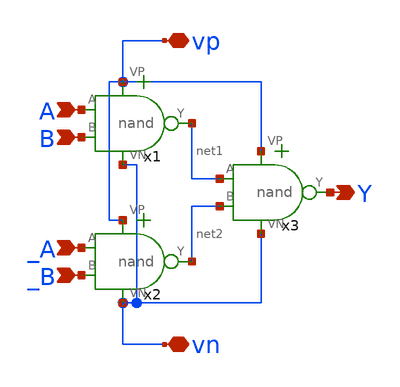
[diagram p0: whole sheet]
** sch_path: xschem/logic_gates/xnor.sch
**.subckt xnor vp vn A B _A _B Y
*.iopin vp
*.iopin vn
*.ipin A
*.ipin B
*.ipin _A
*.ipin _B
*.opin Y
x1 vn A B net1 vp nand
x2 vn _A _B net2 vp nand
x3 vn net1 net2 Y vp nand
**.ends

* expanding   symbol:  /home/madvlsi/dev/git/magic-dds/xschem/logic_gates/nand.sym # of pins=5
** sym_path: xschem/logic_gates/nand.sym
** sch_path: xschem/logic_gates/nand.sch
.subckt nand VN A B Y VP
*.iopin VP
*.iopin VN
*.ipin A
*.ipin B
*.opin Y
XM1 Y A net1 GND sky130_fd_pr__nfet_01v8 L=0.15 W=1 nf=1 ad='int((nf+1)/2) * W/nf * 0.29' as='int((nf+2)/2) * W/nf * 0.29'
+ pd='2*int((nf+1)/2) * (W/nf + 0.29)' ps='2*int((nf+2)/2) * (W/nf + 0.29)' nrd='0.29 / W' nrs='0.29 / W'
+ sa=0 sb=0 sd=0 mult=1 m=1
XM2 net1 B VN GND sky130_fd_pr__nfet_01v8 L=0.15 W=1 nf=1 ad='int((nf+1)/2) * W/nf * 0.29' as='int((nf+2)/2) * W/nf * 0.29'
+ pd='2*int((nf+1)/2) * (W/nf + 0.29)' ps='2*int((nf+2)/2) * (W/nf + 0.29)' nrd='0.29 / W' nrs='0.29 / W'
+ sa=0 sb=0 sd=0 mult=1 m=1
XM3 Y A VP VDD sky130_fd_pr__pfet_01v8 L=0.15 W=1 nf=1 ad='int((nf+1)/2) * W/nf * 0.29' as='int((nf+2)/2) * W/nf * 0.29'
+ pd='2*int((nf+1)/2) * (W/nf + 0.29)' ps='2*int((nf+2)/2) * (W/nf + 0.29)' nrd='0.29 / W' nrs='0.29 / W'
+ sa=0 sb=0 sd=0 mult=1 m=1
XM4 Y B VP VDD sky130_fd_pr__pfet_01v8 L=0.15 W=1 nf=1 ad='int((nf+1)/2) * W/nf * 0.29' as='int((nf+2)/2) * W/nf * 0.29'
+ pd='2*int((nf+1)/2) * (W/nf + 0.29)' ps='2*int((nf+2)/2) * (W/nf + 0.29)' nrd='0.29 / W' nrs='0.29 / W'
+ sa=0 sb=0 sd=0 mult=1 m=1
.ends

.end
